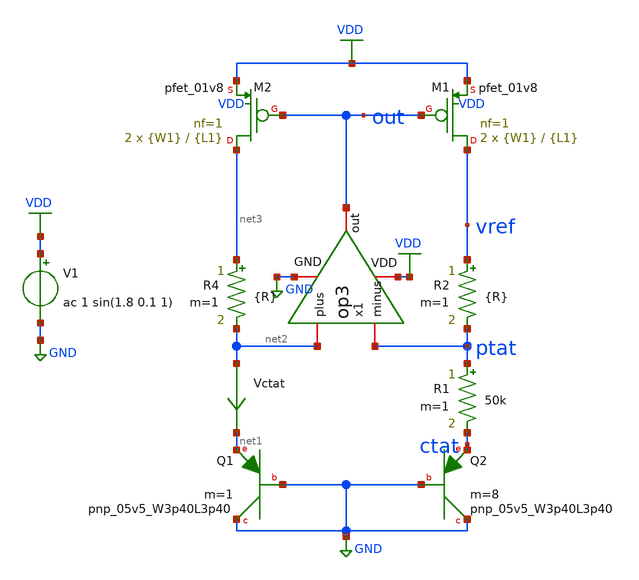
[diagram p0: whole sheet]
** sch_path: xschem/bgr_op3.sch
**.subckt bgr_op3
XQ1 GND GND net1 sky130_fd_pr__pnp_05v5_W3p40L3p40 m=1
XQ2 GND GND ctat sky130_fd_pr__pnp_05v5_W3p40L3p40 m=8
Vctat net2 net1 0
.save i(vctat)
V1 VDD GND ac 1 sin(1.8 0.1 1)
XM1 vref out VDD VDD sky130_fd_pr__pfet_01v8 L={L1} W={W1} nf=1 ad='int((nf+1)/2) * W/nf * 0.29' as='int((nf+2)/2) * W/nf * 0.29'
+ pd='2*int((nf+1)/2) * (W/nf + 0.29)' ps='2*int((nf+2)/2) * (W/nf + 0.29)' nrd='0.29 / W' nrs='0.29 / W'
+ sa=0 sb=0 sd=0 mult=2 m=2
XM2 net3 out VDD VDD sky130_fd_pr__pfet_01v8 L={L1} W={W1} nf=1 ad='int((nf+1)/2) * W/nf * 0.29' as='int((nf+2)/2) * W/nf * 0.29'
+ pd='2*int((nf+1)/2) * (W/nf + 0.29)' ps='2*int((nf+2)/2) * (W/nf + 0.29)' nrd='0.29 / W' nrs='0.29 / W'
+ sa=0 sb=0 sd=0 mult=2 m=2
R1 ptat ctat 50k m=1
R2 vref ptat {R} m=1
R4 net3 net2 {R} m=1
x1 VDD out ptat net2 GND op3
**** begin user architecture code


.param L1=0.15
.param W1=1
.param R=495k



** opencircuitdesign pdks install
.lib $::SKYWATER_MODELS/sky130.lib.spice tt




.option savecurrents
.control
save all
op
remzerovec
write bgr_op3.raw
set appendwrite

dc temp -40 85 1
remzerovec
write bgr_op3.raw
plot (ptat-ctat)
plot ctat
plot vref

********TC********
meas dc temp_avg_vref avg v(vref)
meas dc temp_vref_27 find v(vref) when temp-sweep=27
meas dc temp_pp_vref PP v(vref)
meas dc temp_vref_max max v(vref)
meas dc temp_max_vref when v(vref)='temp_vref_max'
meas dc temp_vref_min min v(vref)
meas dc temp_min_vref when v(vref)='temp_vref_min'
let vref_tc='((temp_pp_vref*1000000)/(125*temp_avg_vref))'
print vref_tc

******PSRR******
ac dec 1000 1 10Meg
write bgr_op3.raw
remzerovec
plot vdb(vref)
meas ac psrr find vdb(vref) at=1k

****Power****
tran 0.1 0.2
write bgr_op3.raw
remzerovec
meas tran ave_v avg vdd
meas tran ave_i avg i(v1)
let ave_power='ave_v*(-ave_i)
*plot vdd vref
*plot -i(v1)
print ave_power

*******LS******
dc v1 0 3.5 0.1
write bgr_op3.raw
remzerovec
plot vdd vref
meas dc vref_max max v(vref) from=1.62 to=1.98
meas dc vref_min min v(vref) from=1.62 to=1.98
let ls='(vref_max-vref_min)/(1.98-1.62)'
print ls

.endc


**** end user architecture code
**.ends

* expanding   symbol:  op3.sym # of pins=5
** sym_path: xschem/op3.sym
** sch_path: xschem/op3.sch
.subckt op3 VDD out minus plus GND
*.iopin VDD
*.iopin GND
*.iopin minus
*.iopin plus
*.iopin out
**** begin user architecture code


**diffpair**
.param L1=1
.param W1=5
.param M1=1

**PMOS**
.param L2=1
.param W2=2
.param M2=1

**NMOS**
.param L3=10
.param W3=1
.param M3=1

**Current control**
.param L4=5
.param W4=2.5
.param M4=1


**** end user architecture code
V4 bias GND dc 0.6
XM1 net2 minus net1 GND sky130_fd_pr__nfet_01v8 L={L1} W={W1} nf=1 ad='int((nf+1)/2) * W/nf * 0.29' as='int((nf+2)/2)
+ * W/nf * 0.29' pd='2*int((nf+1)/2) * (W/nf + 0.29)' ps='2*int((nf+2)/2) * (W/nf + 0.29)' nrd='0.29 /
+ W' nrs='0.29 / W' sa=0 sb=0 sd=0 mult={M1} m={M1}
XM3 net8 bias GND GND sky130_fd_pr__nfet_01v8 L={L4} W={W4} nf=1 ad='int((nf+1)/2) * W/nf * 0.29' as='int((nf+2)/2)
+ * W/nf * 0.29' pd='2*int((nf+1)/2) * (W/nf + 0.29)' ps='2*int((nf+2)/2) * (W/nf + 0.29)' nrd='0.29 /
+ W' nrs='0.29 / W' sa=0 sb=0 sd=0 mult={M4} m={M4}
Vbias net1 net8 0
.save i(vbias)
XM2 net4 plus net1 GND sky130_fd_pr__nfet_01v8 L={L1} W={W1} nf=1 ad='int((nf+1)/2) * W/nf * 0.29' as='int((nf+2)/2)
+ * W/nf * 0.29' pd='2*int((nf+1)/2) * (W/nf + 0.29)' ps='2*int((nf+2)/2) * (W/nf + 0.29)' nrd='0.29 /
+ W' nrs='0.29 / W' sa=0 sb=0 sd=0 mult={M1} m={M1}
XM7 net5 bias2 net2 VDD sky130_fd_pr__pfet_01v8 L={L3} W={W3} nf=1 ad='int((nf+1)/2) * W/nf * 0.29' as='int((nf+2)/2)
+ * W/nf * 0.29' pd='2*int((nf+1)/2) * (W/nf + 0.29)' ps='2*int((nf+2)/2) * (W/nf + 0.29)' nrd='0.29 /
+ W' nrs='0.29 / W' sa=0 sb=0 sd=0 mult={M3} m={M3}
XM8 net5 bias3 net6 GND sky130_fd_pr__nfet_01v8 L={L2} W={W2} nf=1 ad='int((nf+1)/2) * W/nf * 0.29' as='int((nf+2)/2)
+ * W/nf * 0.29' pd='2*int((nf+1)/2) * (W/nf + 0.29)' ps='2*int((nf+2)/2) * (W/nf + 0.29)' nrd='0.29 /
+ W' nrs='0.29 / W' sa=0 sb=0 sd=0 mult={M2} m={M2}
XM9 net6 net5 GND GND sky130_fd_pr__nfet_01v8 L={L2} W={W2} nf=1 ad='int((nf+1)/2) * W/nf * 0.29' as='int((nf+2)/2)
+ * W/nf * 0.29' pd='2*int((nf+1)/2) * (W/nf + 0.29)' ps='2*int((nf+2)/2) * (W/nf + 0.29)' nrd='0.29 /
+ W' nrs='0.29 / W' sa=0 sb=0 sd=0 mult={M2} m={M2}
XM10 out bias3 net7 GND sky130_fd_pr__nfet_01v8 L={L2} W={W2} nf=1 ad='int((nf+1)/2) * W/nf * 0.29' as='int((nf+2)/2)
+ * W/nf * 0.29' pd='2*int((nf+1)/2) * (W/nf + 0.29)' ps='2*int((nf+2)/2) * (W/nf + 0.29)' nrd='0.29 /
+ W' nrs='0.29 / W' sa=0 sb=0 sd=0 mult={M2} m={M2}
XM11 net7 net5 GND GND sky130_fd_pr__nfet_01v8 L={L2} W={W2} nf=1 ad='int((nf+1)/2) * W/nf * 0.29' as='int((nf+2)/2)
+ * W/nf * 0.29' pd='2*int((nf+1)/2) * (W/nf + 0.29)' ps='2*int((nf+2)/2) * (W/nf + 0.29)' nrd='0.29 /
+ W' nrs='0.29 / W' sa=0 sb=0 sd=0 mult={M2} m={M2}
V5 bias1 GND dc 0.6
V6 bias2 GND dc 0.6
V7 bias3 GND dc 0.6
Vbias1 net3 net4 0
.save i(vbias1)
Vbias2 net9 out 0
.save i(vbias2)
XM4 net2 bias1 VDD VDD sky130_fd_pr__pfet_01v8 L={L3} W={W3} nf=1 ad='int((nf+1)/2) * W/nf * 0.29' as='int((nf+2)/2)
+ * W/nf * 0.29' pd='2*int((nf+1)/2) * (W/nf + 0.29)' ps='2*int((nf+2)/2) * (W/nf + 0.29)' nrd='0.29 /
+ W' nrs='0.29 / W' sa=0 sb=0 sd=0 mult={M3} m={M3}
XM5 net9 bias2 net4 VDD sky130_fd_pr__pfet_01v8 L={L3} W={W3} nf=1 ad='int((nf+1)/2) * W/nf * 0.29' as='int((nf+2)/2)
+ * W/nf * 0.29' pd='2*int((nf+1)/2) * (W/nf + 0.29)' ps='2*int((nf+2)/2) * (W/nf + 0.29)' nrd='0.29 /
+ W' nrs='0.29 / W' sa=0 sb=0 sd=0 mult={M3} m={M3}
XM6 net3 bias1 VDD VDD sky130_fd_pr__pfet_01v8 L={L3} W={W3} nf=1 ad='int((nf+1)/2) * W/nf * 0.29' as='int((nf+2)/2)
+ * W/nf * 0.29' pd='2*int((nf+1)/2) * (W/nf + 0.29)' ps='2*int((nf+2)/2) * (W/nf + 0.29)' nrd='0.29 /
+ W' nrs='0.29 / W' sa=0 sb=0 sd=0 mult={M3} m={M3}
.ends

.GLOBAL VDD
.GLOBAL GND
.end
